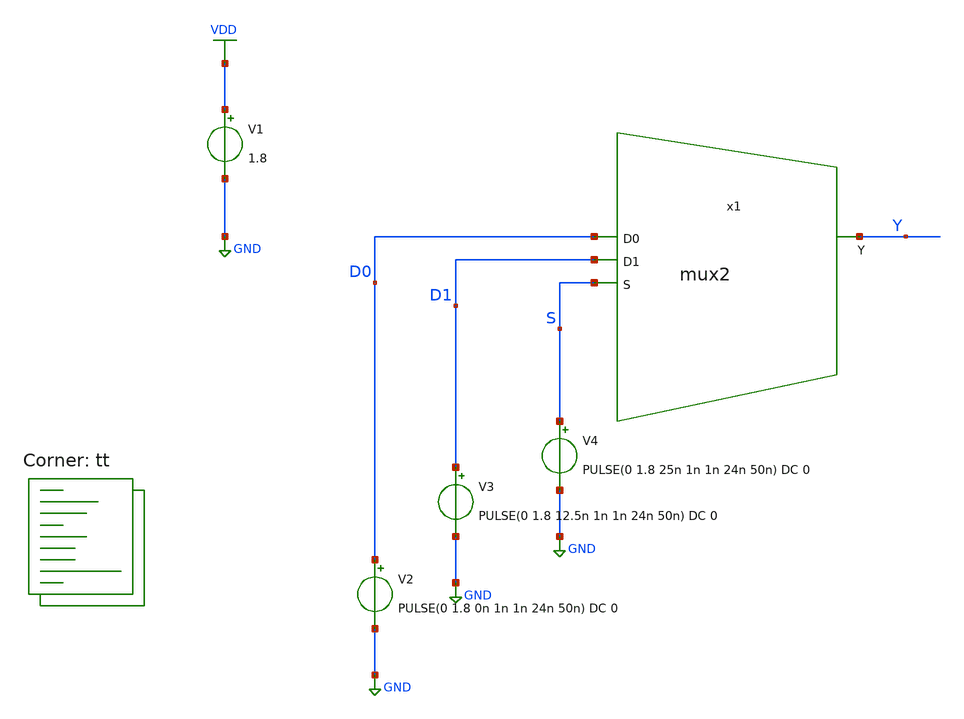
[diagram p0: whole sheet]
** sch_path: eng331lab_final/eng331lab_xschem/tb_mux2.sch
**.subckt tb_mux2
V1 VDD GND 1.8
V2 D0 GND PULSE(0 1.8 0n 1n 1n 24n 50n) DC 0
V3 D1 GND PULSE(0 1.8 12.5n 1n 1n 24n 50n) DC 0
V4 S GND PULSE(0 1.8 25n 1n 1n 24n 50n) DC 0
x1 D0 Y D1 S mux2
**** begin user architecture code
.lib $::SKYWATER_MODELS/sky130.lib.spice tt

.control
  save all
  tran 10n 400n
  write tb_mux2.raw
  set appendwrite
.endc


**** end user architecture code
**.ends

* expanding   symbol:  eng331lab_xschem/mux2.sym # of pins=4
** sym_path: eng331lab_final/eng331lab_xschem/mux2.sym
** sch_path: eng331lab_final/eng331lab_xschem/mux2.sch
.subckt mux2 D0 Y D1 S
*.ipin D0
*.ipin D1
*.ipin S
*.opin Y
x1 D0 out1 s_bar and2
x2 D1 out2 S and2
x3 out1 Y out2 or2
x4 s_bar S inv
.ends


* expanding   symbol:  eng331lab_xschem/and2.sym # of pins=3
** sym_path: eng331lab_final/eng331lab_xschem/and2.sym
** sch_path: eng331lab_final/eng331lab_xschem/and2.sch
.subckt and2 A Y B
*.ipin A
*.ipin B
*.opin Y
x1e A Y_bar B nand2
x2 Y Y_bar inv
.ends


* expanding   symbol:  eng331lab_xschem/or2.sym # of pins=3
** sym_path: eng331lab_final/eng331lab_xschem/or2.sym
** sch_path: eng331lab_final/eng331lab_xschem/or2.sch
.subckt or2 A Y B
*.ipin A
*.ipin B
*.opin Y
x1 A B Y_bar nor2
x2 Y Y_bar inv
.ends


* expanding   symbol:  eng331lab_xschem/inv.sym # of pins=2
** sym_path: eng331lab_final/eng331lab_xschem/inv.sym
** sch_path: eng331lab_final/eng331lab_xschem/inv.sch
.subckt inv Y A
*.ipin A
*.opin Y
XM1 Y A VDD VDD sky130_fd_pr__pfet_01v8 L=0.15 W=0.8 nf=1 ad='int((1 + 1)/2) * 0.8 / 1 * 0.29' as='int((1 + 2)/2) * 0.8 / 1 * 0.29'
+ pd='2*int((1 + 1)/2) * (0.8 / 1 + 0.29)' ps='2*int((1 + 2)/2) * (0.8 / 1 + 0.29)' nrd='0.29 / 0.8 ' nrs='0.29 / 0.8 '
+ sa=0 sb=0 sd=0 mult=1 m=1
XM2 Y A GND GND sky130_fd_pr__nfet_01v8 L=0.15 W=0.5 nf=1 ad='int((1 + 1)/2) * 0.5 / 1 * 0.29' as='int((1 + 2)/2) * 0.5 / 1 * 0.29'
+ pd='2*int((1 + 1)/2) * (0.5 / 1 + 0.29)' ps='2*int((1 + 2)/2) * (0.5 / 1 + 0.29)' nrd='0.29 / 0.5 ' nrs='0.29 / 0.5 '
+ sa=0 sb=0 sd=0 mult=1 m=1
.ends


* expanding   symbol:  eng331_debug/eng331lab_xschem/nand2.sym # of pins=3
** sym_path: eng331lab_final/eng331lab_xschem/nand2.sym
** sch_path: eng331lab_final/eng331lab_xschem/nand2.sch
.subckt nand2 A Y B
*.ipin A
*.ipin B
*.opin Y
XM1 Y A VDD VDD sky130_fd_pr__pfet_01v8 L=0.15 W=0.8 nf=1 ad='int((1 + 1)/2) * 0.8 / 1 * 0.29' as='int((1 + 2)/2) * 0.8 / 1 * 0.29'
+ pd='2*int((1 + 1)/2) * (0.8 / 1 + 0.29)' ps='2*int((1 + 2)/2) * (0.8 / 1 + 0.29)' nrd='0.29 / 0.8 ' nrs='0.29 / 0.8 '
+ sa=0 sb=0 sd=0 mult=1 m=1
XM2 Y B VDD VDD sky130_fd_pr__pfet_01v8 L=0.15 W=0.8 nf=1 ad='int((1 + 1)/2) * 0.8 / 1 * 0.29' as='int((1 + 2)/2) * 0.8 / 1 * 0.29'
+ pd='2*int((1 + 1)/2) * (0.8 / 1 + 0.29)' ps='2*int((1 + 2)/2) * (0.8 / 1 + 0.29)' nrd='0.29 / 0.8 ' nrs='0.29 / 0.8 '
+ sa=0 sb=0 sd=0 mult=1 m=1
XM3 Y A net1 GND sky130_fd_pr__nfet_01v8 L=0.15 W=1 nf=1 ad='int((1 + 1)/2) * 1 / 1 * 0.29' as='int((1 + 2)/2) * 1 / 1 * 0.29'
+ pd='2*int((1 + 1)/2) * (1 / 1 + 0.29)' ps='2*int((1 + 2)/2) * (1 / 1 + 0.29)' nrd='0.29 / 1 ' nrs='0.29 / 1 '
+ sa=0 sb=0 sd=0 mult=1 m=1
XM4 net1 B GND GND sky130_fd_pr__nfet_01v8 L=0.15 W=1 nf=1 ad='int((1 + 1)/2) * 1 / 1 * 0.29' as='int((1 + 2)/2) * 1 / 1 * 0.29'
+ pd='2*int((1 + 1)/2) * (1 / 1 + 0.29)' ps='2*int((1 + 2)/2) * (1 / 1 + 0.29)' nrd='0.29 / 1 ' nrs='0.29 / 1 '
+ sa=0 sb=0 sd=0 mult=1 m=1
.ends


* expanding   symbol:  eng331_debug/eng331lab_xschem/nor2.sym # of pins=3
** sym_path: eng331lab_final/eng331lab_xschem/nor2.sym
** sch_path: eng331lab_final/eng331lab_xschem/nor2.sch
.subckt nor2 A B Y
*.ipin A
*.ipin B
*.opin Y
XM1 net1 A VDD VDD sky130_fd_pr__pfet_01v8 L=0.15 W=1.6 nf=1 ad='int((1 + 1)/2) * 1.6 / 1 * 0.29' as='int((1 + 2)/2) * 1.6 / 1 * 0.29'
+ pd='2*int((1 + 1)/2) * (1.6 / 1 + 0.29)' ps='2*int((1 + 2)/2) * (1.6 / 1 + 0.29)' nrd='0.29 / 1.6 ' nrs='0.29 / 1.6 '
+ sa=0 sb=0 sd=0 mult=1 m=1
XM2 Y B net1 VDD sky130_fd_pr__pfet_01v8 L=0.15 W=1.6 nf=1 ad='int((1 + 1)/2) * 1.6 / 1 * 0.29' as='int((1 + 2)/2) * 1.6 / 1 * 0.29'
+ pd='2*int((1 + 1)/2) * (1.6 / 1 + 0.29)' ps='2*int((1 + 2)/2) * (1.6 / 1 + 0.29)' nrd='0.29 / 1.6 ' nrs='0.29 / 1.6 '
+ sa=0 sb=0 sd=0 mult=1 m=1
XM3 Y A GND GND sky130_fd_pr__nfet_01v8 L=0.15 W=0.5 nf=1 ad='int((1 + 1)/2) * 0.5 / 1 * 0.29' as='int((1 + 2)/2) * 0.5 / 1 * 0.29'
+ pd='2*int((1 + 1)/2) * (0.5 / 1 + 0.29)' ps='2*int((1 + 2)/2) * (0.5 / 1 + 0.29)' nrd='0.29 / 0.5 ' nrs='0.29 / 0.5 '
+ sa=0 sb=0 sd=0 mult=1 m=1
XM4 Y B GND GND sky130_fd_pr__nfet_01v8 L=0.15 W=0.5 nf=1 ad='int((1 + 1)/2) * 0.5 / 1 * 0.29' as='int((1 + 2)/2) * 0.5 / 1 * 0.29'
+ pd='2*int((1 + 1)/2) * (0.5 / 1 + 0.29)' ps='2*int((1 + 2)/2) * (0.5 / 1 + 0.29)' nrd='0.29 / 0.5 ' nrs='0.29 / 0.5 '
+ sa=0 sb=0 sd=0 mult=1 m=1
.ends

.GLOBAL VDD
.GLOBAL GND
.end
